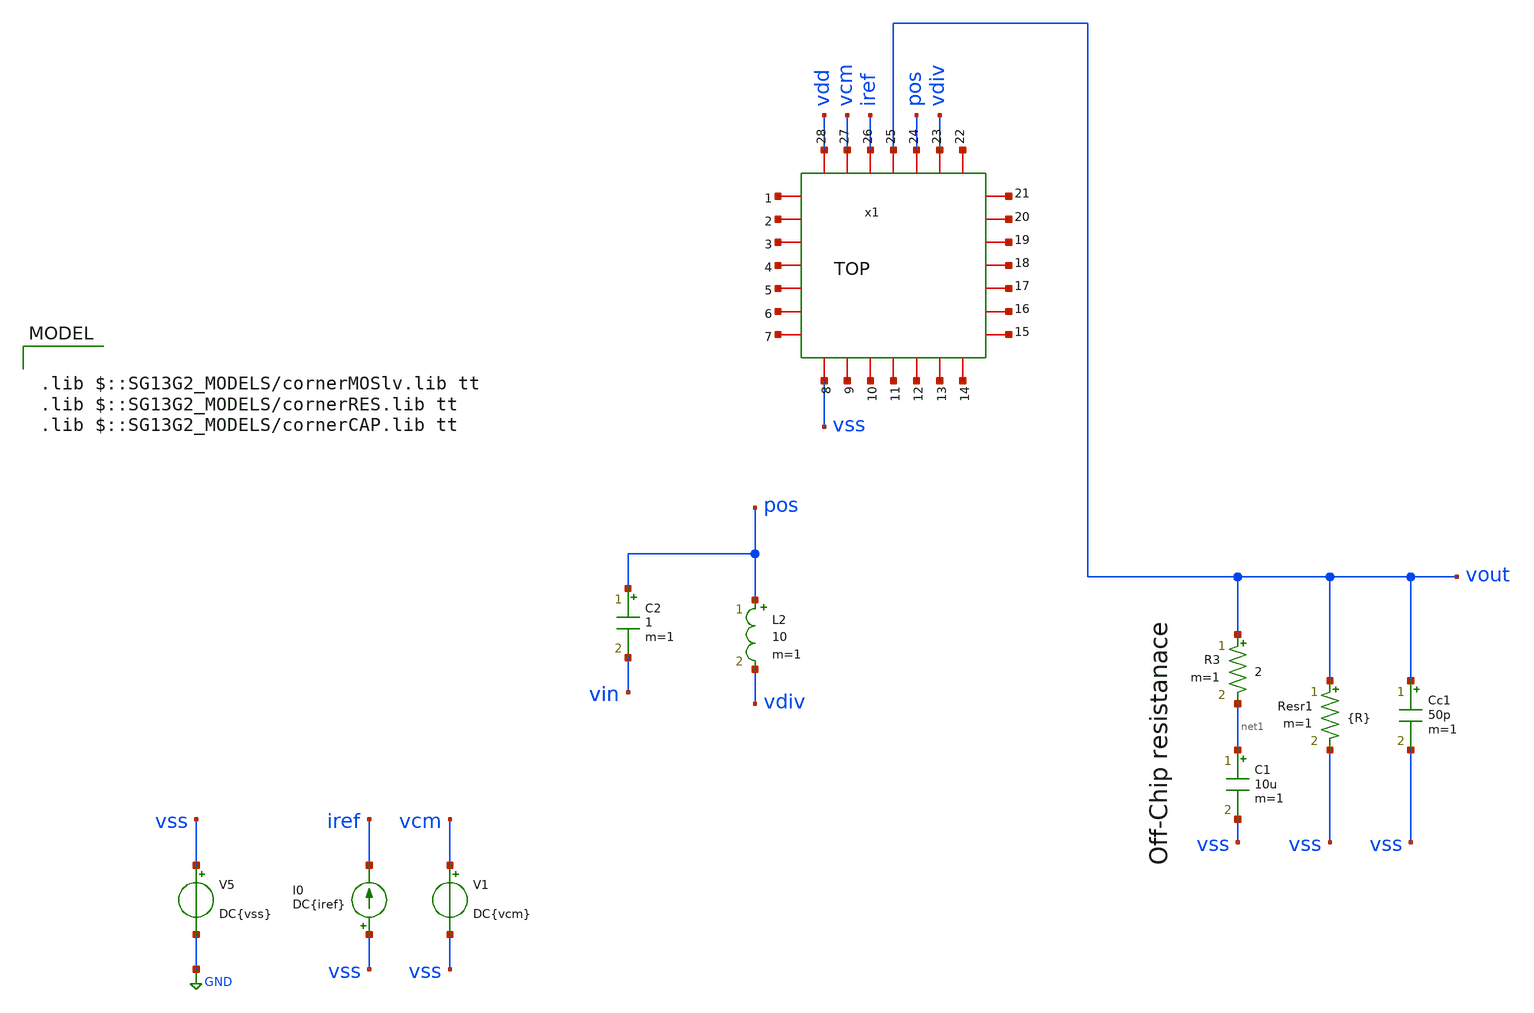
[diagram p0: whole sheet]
** sch_path: AC3E-IHP_ALDO/design_data/xschem/top/TOP_ldo_openloop_tb.sch
**.subckt TOP_ldo_openloop_tb
V1 vcm vss DC{vcm}
V5 vss GND DC{vss}
I0 vss iref DC{iref}
C2 pos vin 1 m=1
L2 pos vdiv 10 m=1
C1 net1 vss 10u m=1
R3 vout net1 2 m=1
Resr1 vout vss {R} m=1
Cc1 vout vss 50p m=1
x1 vdd net2 vdiv pos iref vcm vout net3 net4 net5 net6 net7 net8 net9 net10 net11 net12 net13 net14
+ net15 net16 vss net17 net18 net19 net20 net21 net22 TOP
**** begin user architecture code

.lib $::SG13G2_MODELS/cornerMOSlv.lib tt
.lib $::SG13G2_MODELS/cornerRES.lib tt
.lib $::SG13G2_MODELS/cornerCAP.lib tt




Vs vdd 0 1.8
Vin vin 0 DC 0 AC 1

.end




.control
tran 10n 1u
plot v(vout) v(pos) v(vcm)
.endc
.end

.control
tran 1e-6 1e-3
write test_tran.raw
noise v(vout) Vin dec 333 10 100e3
print inoise_total onoise_total
setplot noise1
plot onoise_spectrum
.endc





*Simulation
.control
pre_osdi /home/ac3e/Documents/psp103_nqs.osdi
reset
  set color0 = white

  ac dec 100 1 10G
  setplot ac1
  meas ac GBW when vdb(vout)=0
  meas ac DCG find vdb(vout) at=1
  meas ac PM find vp(vout) when vdb(vout)=0
  print PM*180/PI
  meas ac GM find vdb(vout) when vp(vout)=0
  plot vdb(vout) {vp(vout)*180/PI}
  write tb_opamp_openloop_ac1.raw

  reset
  op


print @n.x1.xm8.nsg13_lv_nmos[vgs]-@n.x1.xm8.nsg13_lv_nmos[vth]
print @n.x1.xm8.nsg13_lv_nmos[vds]

print @n.x1.XM7.nsg13_lv_nmos[vgs]-@n.x1.XM7.nsg13_lv_nmos[vth]
print @n.x1.XM7.nsg13_lv_nmos[vds]
print @n.x1.XM7.nsg13_lv_nmos[ids]

print @n.x1.xm6.nsg13_lv_pmos[vgs]-@n.x1.xm6.nsg13_lv_pmos[vth]
print @n.x1.xm6.nsg13_lv_pmos[vds]
print @n.x1.xm6.nsg13_lv_pmos[gm]
print @n.x1.xm6.nsg13_lv_pmos[gm]/@n.x1.xm6.nsg13_lv_pmos[ids]
print @n.x1.xm6.nsg13_lv_pmos[gm]/@n.x1.xm6.nsg13_lv_pmos[gds]

print @n.x1.xm5.nsg13_lv_nmos[vgs]-@n.x1.xm5.nsg13_lv_nmos[vth]
print @n.x1.xm5.nsg13_lv_nmos[vds]
print @n.x1.xm5.nsg13_lv_nmos[ids]

print @n.x1.xm1.nsg13_lv_nmos[vgs]-@n.x1.xm1.nsg13_lv_nmos[vth]
print @n.x1.xm1.nsg13_lv_nmos[vds]
print @n.x1.xm1.nsg13_lv_nmos[gm]

print @n.x1.xm2.nsg13_lv_nmos[vgs]-@n.x1.xm2.nsg13_lv_nmos[vth]
print @n.x1.xm2.nsg13_lv_nmos[vds]
print @n.x1.xm2.nsg13_lv_nmos[gm]

print @n.x1.xm3.nsg13_lv_pmos[vgs]-@n.x1.xm3.nsg13_lv_pmos[vth]
print @n.x1.xm3.nsg13_lv_pmos[vds]
print @n.x1.xm3.nsg13_lv_pmos[ids]

print @n.x1.xm4.nsg13_lv_pmos[vgs]-@n.x1.xm4.nsg13_lv_pmos[vth]
print @n.x1.xm4.nsg13_lv_pmos[vds]
print @n.x1.xm4.nsg13_lv_pmos[ids]

print v(vout)
print v(pos)

  setplot op1
  unset filetype
  write tb_opamp_openloop.raw

.endc

.end





.param iref = 5u
.param vdd  = 1.8
.param vss  = 0.0
.param vcm  = 0.9
.param vac  = 60m

.param w857 = 6u
.param l857 = 2u

.param wpar = 15u
.param lpar = 2u
.param mpar = 1

.param w34  = 2u
.param l34  = 1u
.param m34  = 1

.param w6   = 20u
.param l6   = 0.5u
.param m6   = 1

.param w7   = w857*4
.param w5   = w857*1

.end




.param R=12
*R10 vout 0 {R}
*IL vout 0 PWL(0 0.1m 10u 0.1m 20u 10m 30u 10m)
*CL vout 0 50p

.end


**** end user architecture code
**.ends
.GLOBAL GND
.end
